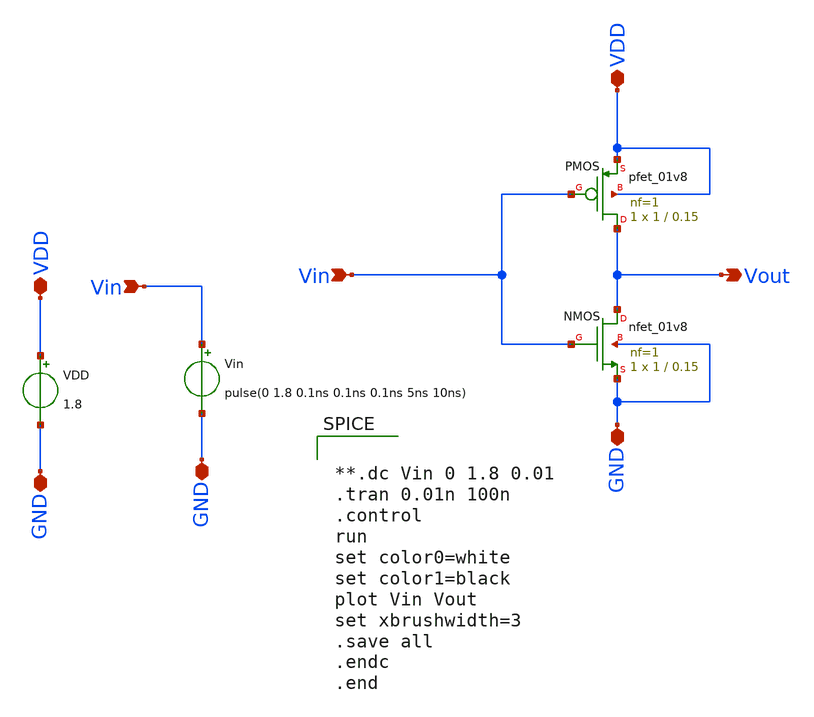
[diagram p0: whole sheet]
** sch_path: Week_0/Inverter_PreLayout/Inverter_tran.sch
**.subckt Inverter_tran Vout Vin Vin VDD GND GND GND VDD
*.opin Vout
*.ipin Vin
*.ipin Vin
*.iopin VDD
*.iopin GND
*.iopin GND
*.iopin GND
*.iopin VDD
XPMOS Vout Vin VDD VDD sky130_fd_pr__pfet_01v8 L=0.15 W=1 nf=1 ad='int((nf+1)/2) * W/nf * 0.29' as='int((nf+2)/2) * W/nf * 0.29'
+ pd='2*int((nf+1)/2) * (W/nf + 0.29)' ps='2*int((nf+2)/2) * (W/nf + 0.29)' nrd='0.29 / W' nrs='0.29 / W'
+ sa=0 sb=0 sd=0 mult=1 m=1
XNMOS Vout Vin GND GND sky130_fd_pr__nfet_01v8 L=0.15 W=1 nf=1 ad='int((nf+1)/2) * W/nf * 0.29' as='int((nf+2)/2) * W/nf * 0.29'
+ pd='2*int((nf+1)/2) * (W/nf + 0.29)' ps='2*int((nf+2)/2) * (W/nf + 0.29)' nrd='0.29 / W' nrs='0.29 / W'
+ sa=0 sb=0 sd=0 mult=1 m=1
Vin Vin GND pulse(0 1.8 0.1ns 0.1ns 0.1ns 5ns 10ns)
VDD VDD GND 1.8
**** begin user architecture code


**.dc Vin 0 1.8 0.01
.tran 0.01n 100n
.control
run
set color0=white
set color1=black
plot Vin Vout
set xbrushwidth=3
.save all
.endc
.end




.lib /home/swagatika/open_pdks/sky130/sky130A/libs.tech/ngspice/sky130.lib.spice tt

.save all



**** end user architecture code
**.ends
.end
